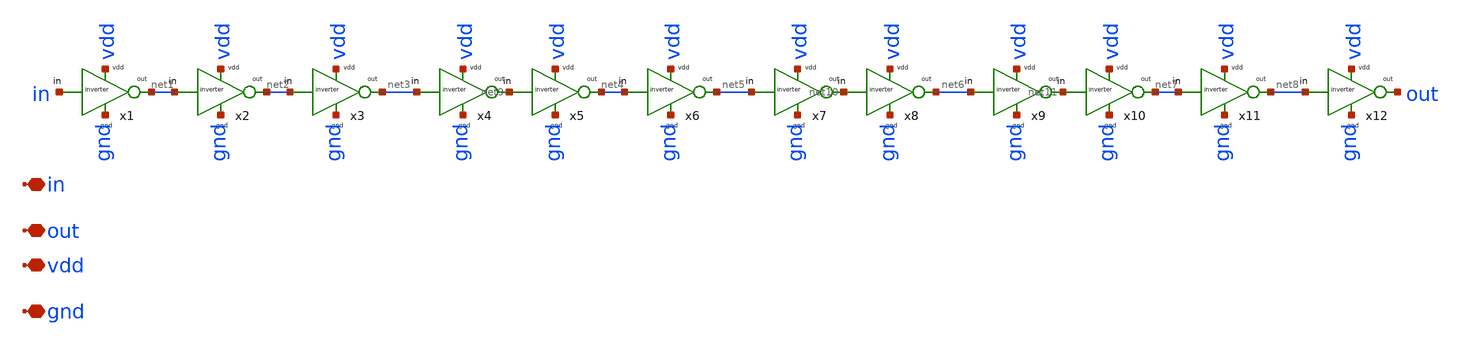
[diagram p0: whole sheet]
** sch_path: Clock_gen_using_transistor_hv/buffer.sch
**.subckt buffer in out vdd gnd
*.iopin in
*.iopin out
*.iopin vdd
*.iopin gnd
x1 in net1 vdd gnd inverter
x2 net1 net2 vdd gnd inverter
x3 net2 net3 vdd gnd inverter
x4 net3 net9 vdd gnd inverter
x5 net9 net4 vdd gnd inverter
x6 net4 net5 vdd gnd inverter
x7 net5 net10 vdd gnd inverter
x8 net10 net6 vdd gnd inverter
x9 net6 net11 vdd gnd inverter
x10 net11 net7 vdd gnd inverter
x11 net7 net8 vdd gnd inverter
x12 net8 out vdd gnd inverter
**.ends

* expanding   symbol:
*+  /home/designer/shared/uni_cass/final_Design_file/Clock_gen_using_transistor_hv/inverter.sym # of pins=4
** sym_path: /home/designer/shared/uni_cass/final_Design_file/Clock_gen_using_transistor_hv/inverter.sym
** sch_path: /home/designer/shared/uni_cass/final_Design_file/Clock_gen_using_transistor_hv/inverter.sch
.subckt inverter in out vdd gnd
*.iopin in
*.iopin vdd
*.iopin out
*.iopin gnd
XM3 out in vdd vdd sg13_hv_pmos w=2u l=2u ng=1 m=1 mm_ok=1
XM1 out in gnd gnd sg13_hv_nmos w=1u l=1u ng=1 m=1 mm_ok=1
.ends

.end
